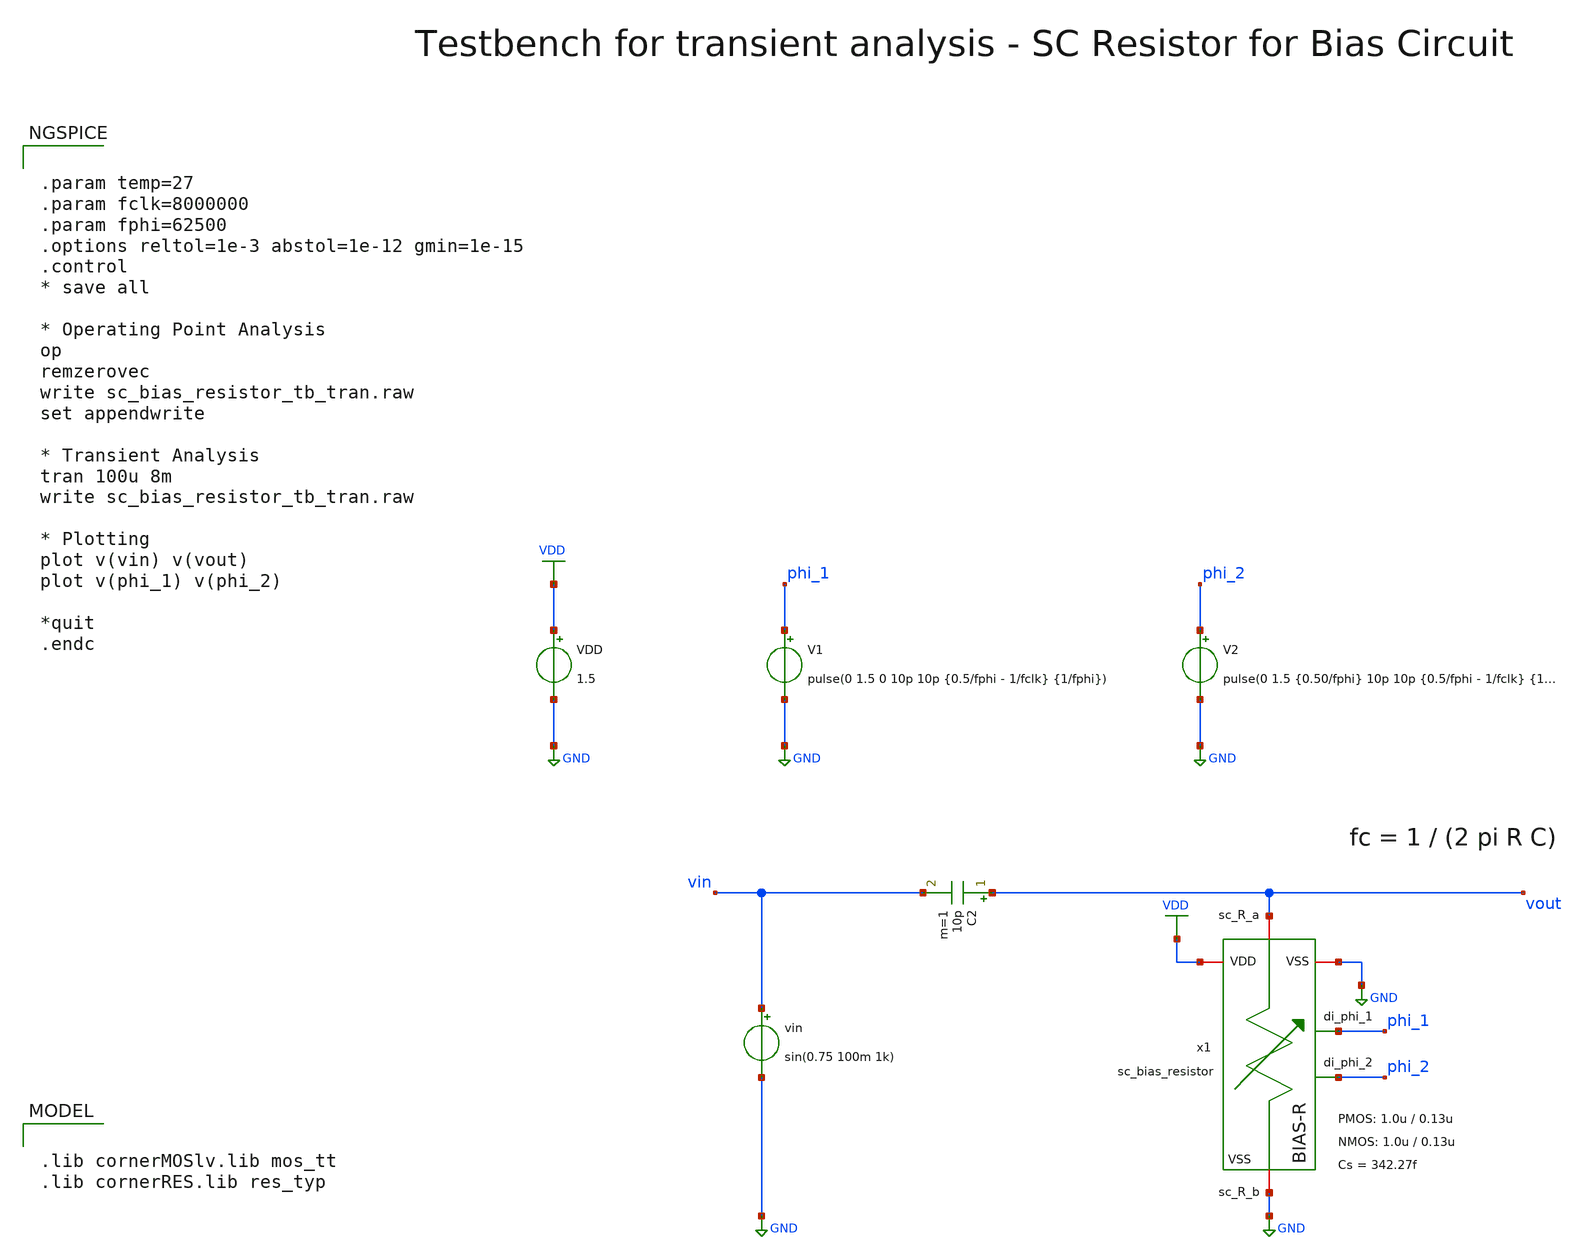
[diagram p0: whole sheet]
** sch_path: SG13G2_ATBS-ADC-main/xschem/bio_amplifier/amplifier_core/bias_circuit/sc_bias_resistor/testbenches/sc_bias_resistor_tb_tran.sch
**.subckt sc_bias_resistor_tb_tran
VDD VDD GND 1.5
V1 phi_1 GND pulse(0 1.5 0 10p 10p {0.5/fphi - 1/fclk} {1/fphi})
V2 phi_2 GND pulse(0 1.5 {0.50/fphi} 10p 10p {0.5/fphi - 1/fclk} {1/fphi})
vin vin GND sin(0.75 100m 1k)
C2 vout vin 10p m=1
x1 vout GND phi_2 phi_1 VDD GND sc_bias_resistor W_P_R=1.0u L_P_R=0.13u W_N_R=1.0u L_N_R=0.13u
+ Cs=342.27f
**** begin user architecture code

.lib cornerMOSlv.lib mos_tt
.lib cornerRES.lib res_typ



.param temp=27
.param fclk=8000000
.param fphi=62500
.options reltol=1e-3 abstol=1e-12 gmin=1e-15
.control
* save all

* Operating Point Analysis
op
remzerovec
write sc_bias_resistor_tb_tran.raw
set appendwrite

* Transient Analysis
tran 100u 8m
write sc_bias_resistor_tb_tran.raw

* Plotting
plot v(vin) v(vout)
plot v(phi_1) v(phi_2)

*quit
.endc

**** end user architecture code
**.ends

* expanding   symbol:
*+  bio_amplifier/amplifier_core/bias_circuit/sc_bias_resistor/sc_bias_resistor.sym # of pins=6
** sym_path: SG13G2_ATBS-ADC-main/xschem/bio_amplifier/amplifier_core/bias_circuit/sc_bias_resistor/sc_bias_resistor.sym
** sch_path: SG13G2_ATBS-ADC-main/xschem/bio_amplifier/amplifier_core/bias_circuit/sc_bias_resistor/sc_bias_resistor.sch
.subckt sc_bias_resistor sc_R_a sc_R_b di_phi_2 di_phi_1 VDD VSS  W_P_R=1.0u L_P_R=0.13u W_N_R=1.0u
+ L_N_R=0.13u Cs=100f
*.iopin VSS
*.iopin VDD
*.iopin sc_R_a
*.iopin sc_R_b
*.ipin di_phi_1
*.ipin di_phi_2
C1 net1 sc_R_b Cs m=1
x1 VDD di_phi_1 VSS net1 sc_R_a di_phi_1_n transmission_gate_lv_wo_dummy W_P=W_P_R L_P=L_P_R
+ W_N=W_N_R L_N=L_N_R
x2 VDD di_phi_2 VSS sc_R_b net1 di_phi_2_n transmission_gate_lv_wo_dummy W_P=W_P_R L_P=L_P_R
+ W_N=W_N_R L_N=L_N_R
C2 net2 sc_R_b Cs m=1
x3 VDD di_phi_2 VSS net2 sc_R_a di_phi_2_n transmission_gate_lv_wo_dummy W_P=W_P_R L_P=L_P_R
+ W_N=W_N_R L_N=L_N_R
x4 VDD di_phi_1 VSS sc_R_b net2 di_phi_1_n transmission_gate_lv_wo_dummy W_P=W_P_R L_P=L_P_R
+ W_N=W_N_R L_N=L_N_R
x5 VDD di_phi_1 di_phi_1_n VSS inverter_lv W_P=W_P_R L_P=L_P_R W_N=W_N_R L_N=L_N_R
x6 VDD di_phi_2 di_phi_2_n VSS inverter_lv W_P=W_P_R L_P=L_P_R W_N=W_N_R L_N=L_N_R
.ends


* expanding   symbol:  transmission_gate/transmission_gate_lv_wo_dummy.sym # of pins=6
** sym_path: SG13G2_ATBS-ADC-main/xschem/transmission_gate/transmission_gate_lv_wo_dummy.sym
** sch_path: SG13G2_ATBS-ADC-main/xschem/transmission_gate/transmission_gate_lv_wo_dummy.sch
.subckt transmission_gate_lv_wo_dummy VDD di_tg_ctrl VSS v_b v_a di_tg_ctrl_n  W_P=1.0u L_P=0.13u
+ W_N=1.0u L_N=0.13u
*.iopin v_a
*.iopin v_b
*.iopin VDD
*.iopin VSS
*.ipin di_tg_ctrl
*.ipin di_tg_ctrl_n
XM1 v_a di_tg_ctrl v_b VSS sg13_lv_nmos w=W_N l=L_N ng=1 m=1 mm_ok=1
XM2 v_a di_tg_ctrl_n v_b VDD sg13_lv_pmos w=W_P l=L_P ng=1 m=1 mm_ok=1
.ends


* expanding   symbol:  inverter/inverter_lv.sym # of pins=4
** sym_path: SG13G2_ATBS-ADC-main/xschem/inverter/inverter_lv.sym
** sch_path: SG13G2_ATBS-ADC-main/xschem/inverter/inverter_lv.sch
.subckt inverter_lv VDD vin vout VSS  W_P=3.0u L_P=0.13u W_N=1.0u L_N=0.13u
*.ipin vin
*.iopin VDD
*.iopin VSS
*.opin vout
XM1 vout vin VDD VDD sg13_lv_pmos w=W_P l=L_P ng=1 m=1 mm_ok=1
XM2 vout vin VSS VSS sg13_lv_nmos w=W_N l=L_N ng=1 m=1 mm_ok=1
.ends

.GLOBAL GND
.GLOBAL VDD
.end
